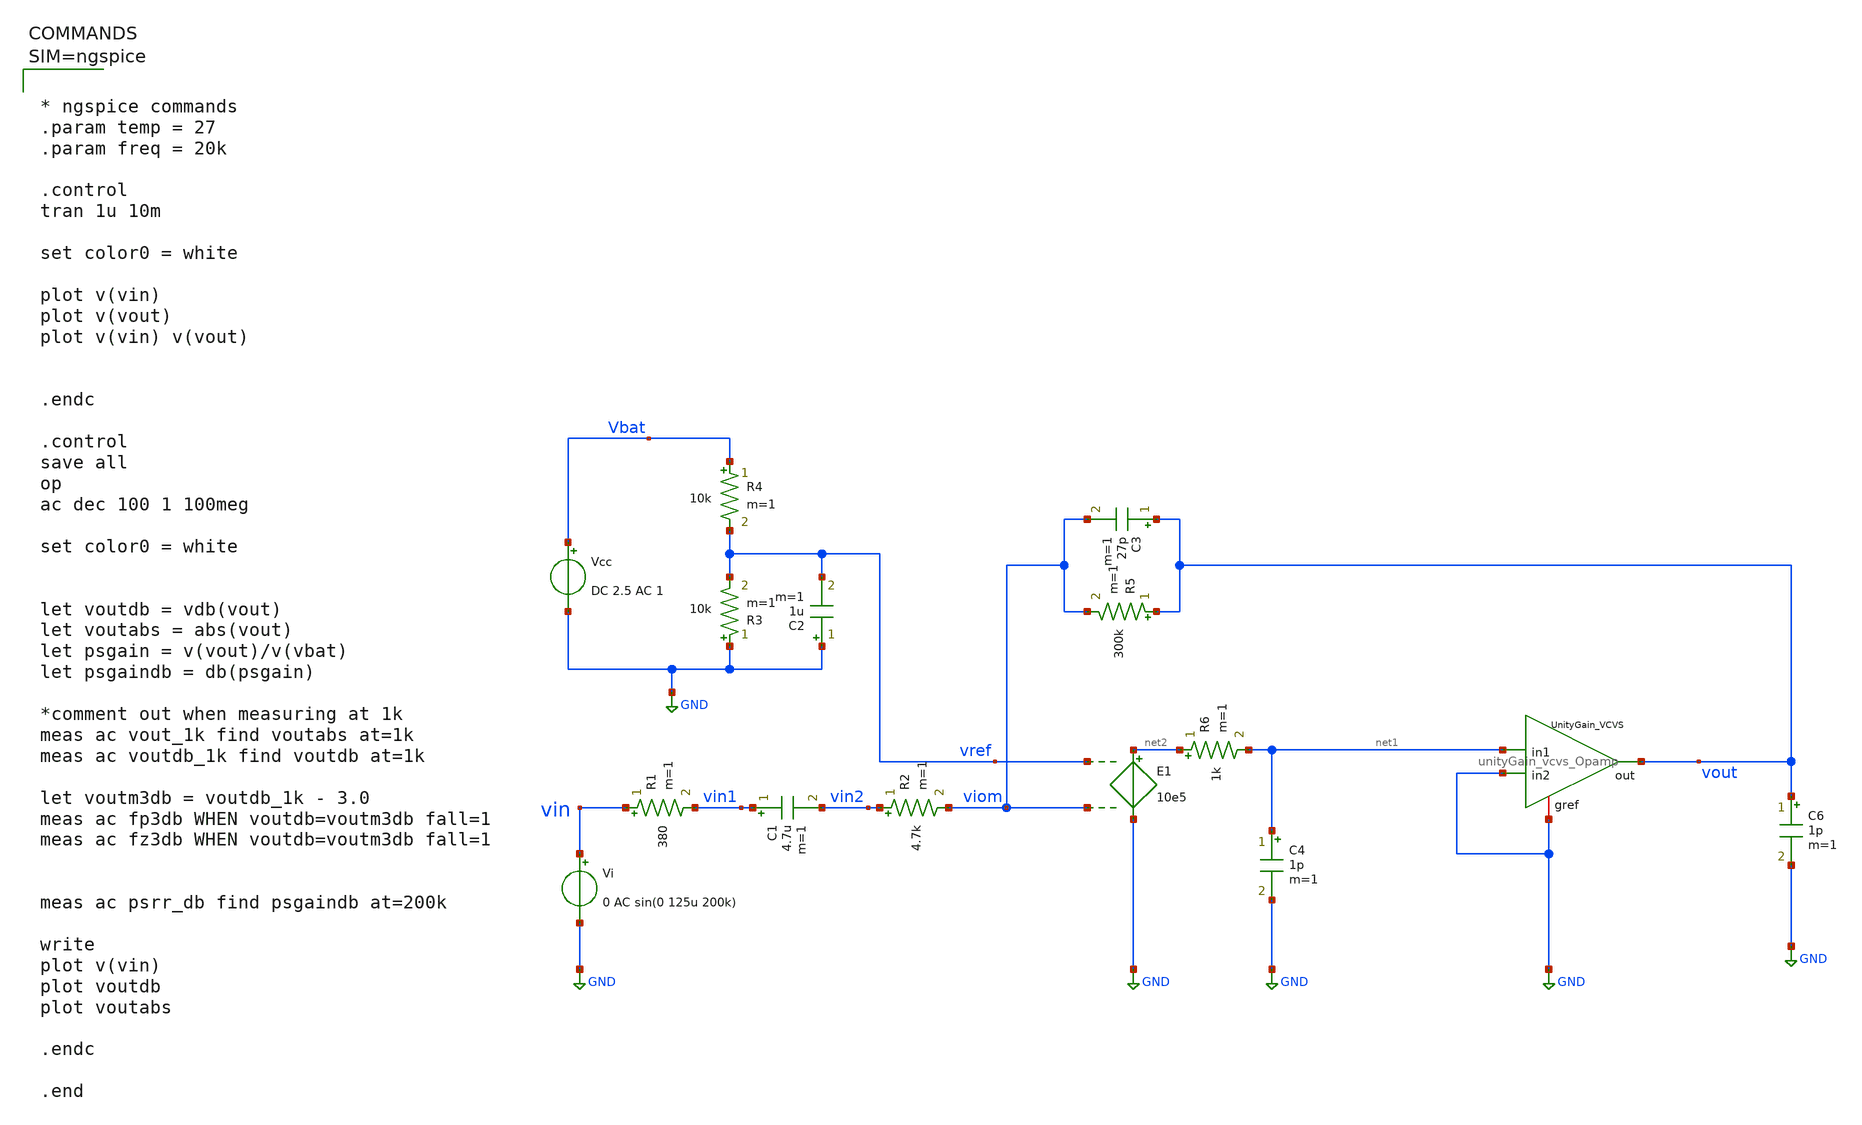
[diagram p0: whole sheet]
** sch_path: testbenches/MEMS_mic_singlePole_with_Symbol.sch
**.subckt MEMS_mic_singlePole_with_Symbol
R1 vin vin1 380 m=1
C1 vin1 vin2 4.7u m=1
R2 vin2 viom 4.7k m=1
E1 net2 GND vref viom 10e5
Vi vin GND 0 AC sin(0 125u 200k)
R3 GND vref 10k m=1
C2 GND vref 1u m=1
R4 Vbat vref 10k m=1
Vcc Vbat GND DC 2.5 AC 1
R5 vout viom 300k m=1
C3 vout viom 27p m=1
C4 net1 GND 1p m=1
C6 vout GND 1p m=1
R6 net2 net1 1k m=1
x1 vout net1 GND GND unityGain_vcvs_Opamp
**** begin user architecture code



* ngspice commands
.param temp = 27
.param freq = 20k

.control
tran 1u 10m

set color0 = white

plot v(vin)
plot v(vout)
plot v(vin) v(vout)


.endc

.control
save all
op
ac dec 100 1 100meg

set color0 = white


let voutdb = vdb(vout)
let voutabs = abs(vout)
let psgain = v(vout)/v(vbat)
let psgaindb = db(psgain)

*comment out when measuring at 1k
meas ac vout_1k find voutabs at=1k
meas ac voutdb_1k find voutdb at=1k

let voutm3db = voutdb_1k - 3.0
meas ac fp3db WHEN voutdb=voutm3db fall=1
meas ac fz3db WHEN voutdb=voutm3db fall=1


meas ac psrr_db find psgaindb at=200k

write
plot v(vin)
plot voutdb
plot voutabs

.endc

.end



**** end user architecture code
**.ends

* expanding   symbol:  unityGain_vcvs_Opamp.sym # of pins=4
** sym_path: sch/unityGain_vcvs_Opamp.sym
** sch_path: sch/unityGain_vcvs_Opamp.sch
.subckt unityGain_vcvs_Opamp out in1 in2 gref
*.ipin in1
*.ipin in2
*.iopin gref
*.opin out
E1 out gref in1 in2 1
.ends

.GLOBAL GND
.end
